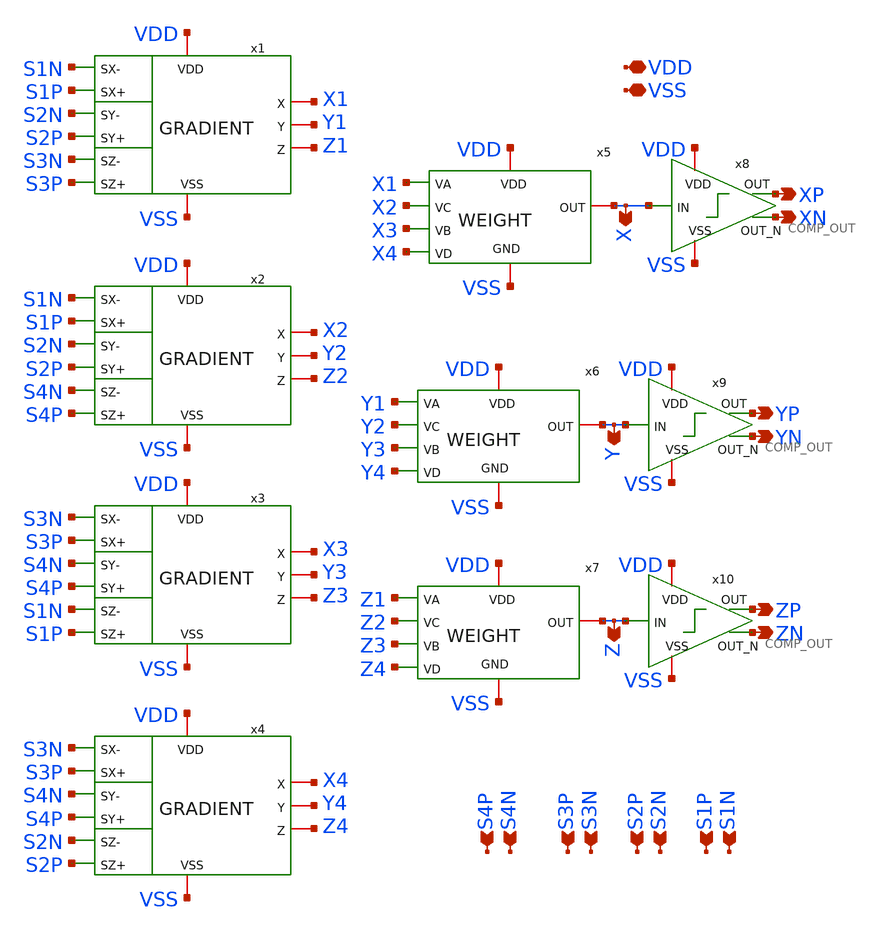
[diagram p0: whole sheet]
** sch_path: FINAL/XSCHEM/GRADIENT_NAV.sch
**.subckt GRADIENT_NAV S1N VDD XN VSS S1P S2N S2P S3N S3P S4N S4P XP YN YP ZN ZP X Y Z
*.ipin S1N
*.iopin VDD
*.opin XN
*.iopin VSS
*.ipin S1P
*.ipin S2N
*.ipin S2P
*.ipin S3N
*.ipin S3P
*.ipin S4N
*.ipin S4P
*.opin XP
*.opin YN
*.opin YP
*.opin ZN
*.opin ZP
*.opin X
*.opin Y
*.opin Z
x1 S1N S1P VDD X1 S2N Y1 Z1 S2P VSS S3N S3P GRADIENT
x2 S1N S1P VDD X2 S2N Y2 Z2 S2P VSS S4N S4P GRADIENT
x3 S3N S3P VDD X3 S4N Y3 Z3 S4P VSS S1N S1P GRADIENT
x4 S3N S3P VDD X4 S4N Y4 Z4 S4P VSS S2N S2P GRADIENT
x5 VDD VSS X X1 X2 X3 X4 WEIGHT
x6 VDD VSS Y Y1 Y2 Y3 Y4 WEIGHT
x7 VDD VSS Z Z1 Z2 Z3 Z4 WEIGHT
x8 VDD XP X XN VSS COMP_OUT
x9 VDD YP Y YN VSS COMP_OUT
x10 VDD ZP Z ZN VSS COMP_OUT
**.ends
.end
